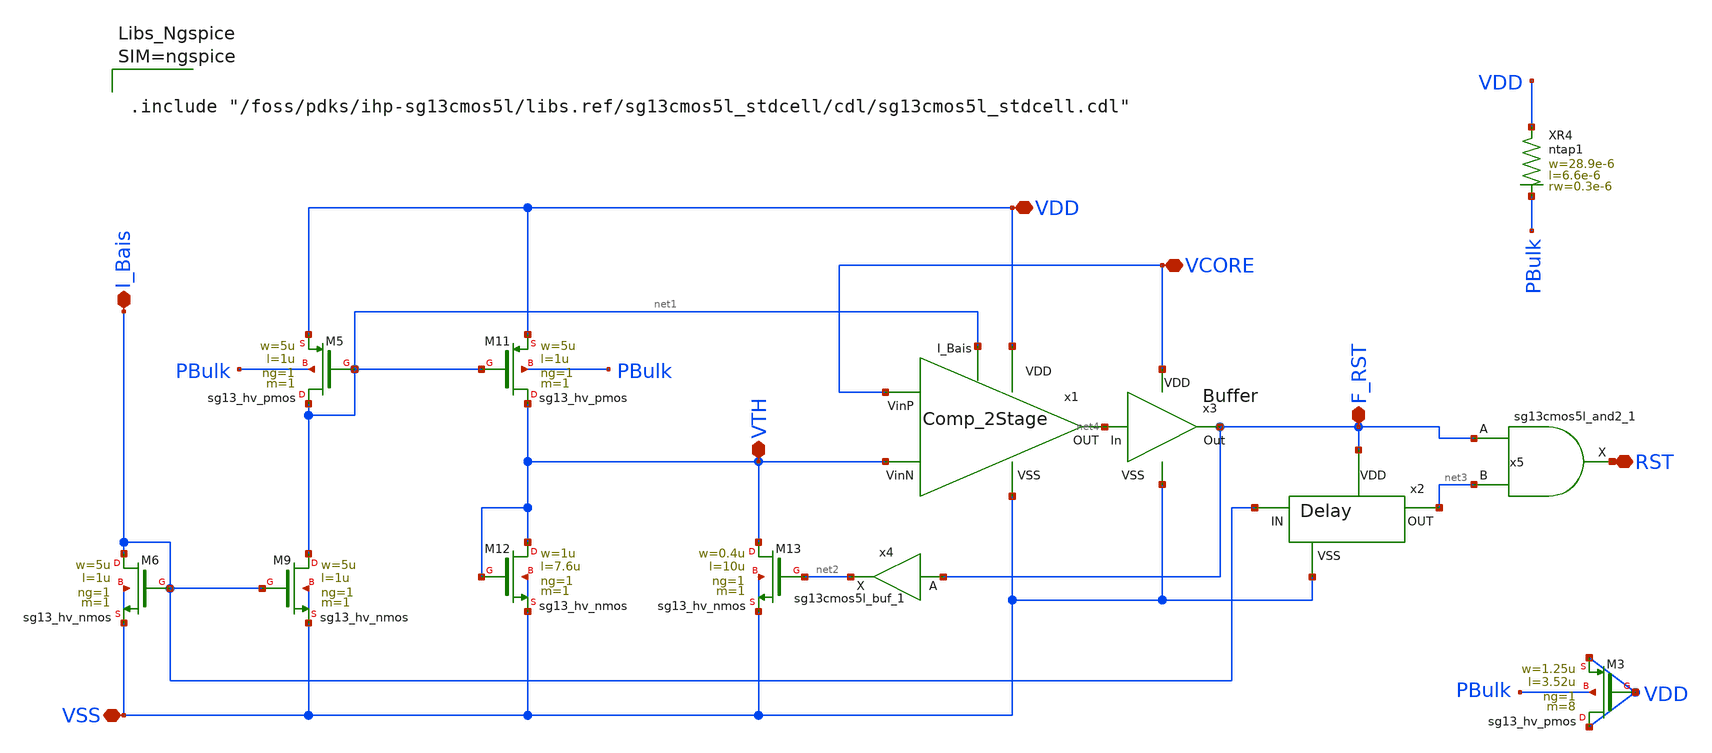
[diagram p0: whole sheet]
** sch_path: LVS/LVS_Sch/LPVSV_Pex.sch
**.subckt LPVSV_Pex VDD VSS I_Bais VTH RST VCORE F_RST
*.iopin VDD
*.iopin VSS
*.iopin I_Bais
*.iopin VTH
*.iopin RST
*.iopin VCORE
*.iopin F_RST
XR4 VDD PBulk ntap1 R=3.265 w=28.9e-6 l=6.6e-6 rw=0.3e-6
XM3 VDD VDD VDD PBulk sg13_hv_pmos w=1.25u l=3.52u ng=1 m=8 mm_ok=1
XM5 net1 net1 VDD PBulk sg13_hv_pmos w=5u l=1u ng=1 m=1 mm_ok=1
XM9 net1 I_Bais VSS VSS sg13_hv_nmos w=5u l=1u ng=1 m=1 mm_ok=1
XM11 VTH net1 VDD PBulk sg13_hv_pmos w=5u l=1u ng=1 m=1 mm_ok=1
XM12 VTH VTH VSS VSS sg13_hv_nmos w=1u l=7.6u ng=1 m=1 mm_ok=1
XM13 VTH net2 VSS VSS sg13_hv_nmos w=0.4u l=10u ng=1 m=1 mm_ok=1
XM6 I_Bais I_Bais VSS VSS sg13_hv_nmos w=5u l=1u ng=1 m=1 mm_ok=1
x4 net2 F_RST VTH VSS sg13cmos5l_buf_1
x1 VDD net1 VCORE VTH net4 VSS Comp_2Stage
x2 F_RST net3 I_Bais VSS Delay
x3 VCORE net4 F_RST VSS Buffer
x5 RST F_RST net3 VCORE VSS sg13cmos5l_and2_1
**** begin user architecture code



.include "/foss/pdks/ihp-sg13cmos5l/libs.ref/sg13cmos5l_stdcell/cdl/sg13cmos5l_stdcell.cdl"



**** end user architecture code
**.ends

* expanding   symbol:  /foss/designs/LPVSV_Chipalooza_2/GDS/LVS_Sch/Comp_2Stage.sym # of pins=6
** sym_path: LVS/LVS_Sch/Comp_2Stage.sym
** sch_path: LVS/LVS_Sch/Comp_2Stage.sch
.subckt Comp_2Stage VDD I_Bais VinP VinN OUT VSS
*.iopin OUT
*.iopin VSS
*.iopin VDD
*.iopin VinP
*.iopin VinN
*.iopin I_Bais
XM2 net1 net1 VSS VSS sg13_hv_nmos w=5u l=10u ng=1 m=2 mm_ok=1
XM4 net2 net1 VSS VSS sg13_hv_nmos w=5u l=10u ng=1 m=2 mm_ok=1
XM1 net1 VinN net3 PBulk1 sg13_hv_pmos w=20u l=2u ng=2 m=2 mm_ok=1
XM3 net2 VinP net3 PBulk1 sg13_hv_pmos w=20u l=2u ng=2 m=2 mm_ok=1
XM8 VDD VDD VDD PBulk1 sg13_hv_pmos w=20u l=2u ng=2 m=4 mm_ok=1
XR2 VDD PBulk1 ntap1 R=2.189 w=27.1e-6 l=25.55e-6 rw=0.3e-6
XM6 OUT net2 VSS VSS sg13_hv_nmos w=5u l=10u ng=1 m=4 mm_ok=1
XM7 net3 I_Bais VDD PBulk sg13_hv_pmos w=5u l=1u ng=1 m=1 mm_ok=1
XM10 OUT I_Bais VDD PBulk sg13_hv_pmos w=5u l=1u ng=1 m=1 mm_ok=1
XM11 VDD VDD VDD PBulk sg13_hv_pmos w=2.5u l=1u ng=1 m=4 mm_ok=1
XR4 VDD PBulk ntap1 R=5.559 w=11.4e-6 l=9.7e-6 rw=0.3e-6
.ends


* expanding   symbol:  /foss/designs/LPVSV_Chipalooza_2/GDS/LVS_Sch/Delay.sym # of pins=4
** sym_path: LVS/LVS_Sch/Delay.sym
** sch_path: LVS/LVS_Sch/Delay.sch
.subckt Delay VDD OUT IN VSS
*.iopin VDD
*.iopin OUT
*.iopin VSS
*.iopin IN
XM7 OUT D VDD PBulk sg13_lv_pmos w=0.8u l=1u ng=1 m=1 mm_ok=1
XM8 VSS OUT VSS PBulk1 sg13_lv_pmos w=10u l=10u ng=1 m=6 mm_ok=1
XM10 D IN VSS VSS sg13_hv_nmos w=0.5u l=10u ng=1 m=1 mm_ok=1
XM2 D D VDD PBulk sg13_lv_pmos w=0.8u l=1u ng=1 m=24 mm_ok=1
XR4 VDD PBulk ntap1 R=4.012 w=16.2e-6 l=12.8e-6 rw=0.3e-6
XR3 VSS PBulk1 ntap1 R=1.423 w=68.1e-6 l=12.6e-6 rw=0.3e-6
XM1 VSS VSS VSS PBulk1 sg13_lv_pmos w=10u l=0.5u ng=1 m=2 mm_ok=1
XM3 VDD VDD VDD PBulk sg13_lv_pmos w=0.8u l=1u ng=1 m=24 mm_ok=1
.ends


* expanding   symbol:  /foss/designs/LPVSV_Chipalooza_2/GDS/LVS_Sch/Buffer.sym # of pins=4
** sym_path: LVS/LVS_Sch/Buffer.sym
** sch_path: LVS/LVS_Sch/Buffer.sch
.subckt Buffer VDD In Out VSS
*.iopin In
*.iopin Out
*.iopin VDD
*.iopin VSS
XM4 net1 In VSS VSS sg13_hv_nmos w=1u l=1.25u ng=1 m=1 mm_ok=1
XM5 Out net1 VSS VSS sg13_hv_nmos w=1u l=1.25u ng=1 m=1 mm_ok=1
XM6 net1 In VDD PBulk sg13_hv_pmos w=3u l=1.25u ng=1 m=1 mm_ok=1
XM7 Out net1 VDD PBulk sg13_hv_pmos w=3u l=1.25u ng=1 m=1 mm_ok=1
XR4 VDD PBulk ntap1 R=7.969 w=10.1e-6 l=4.8e-6 rw=0.3e-6
.ends

.end
